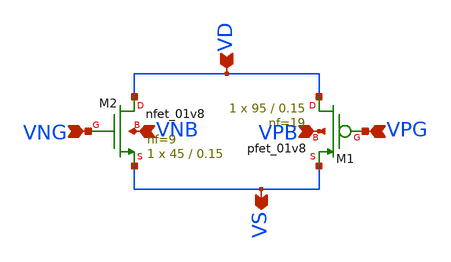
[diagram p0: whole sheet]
** sch_path: SP23_Tapeout/C2S2_Analog_TestChip-main/xschem/a_mux_switch.sch
**.subckt a_mux_switch VPG VNG VD VS VPB VNB
*.ipin VPG
*.ipin VNG
*.ipin VD
*.opin VS
*.ipin VPB
*.ipin VNB
XM1 VD VPG VS VPB sky130_fd_pr__pfet_01v8 L=0.15 W=95 nf=19 ad='int((nf+1)/2) * W/nf * 0.29' as='int((nf+2)/2) * W/nf * 0.29'
+ pd='2*int((nf+1)/2) * (W/nf + 0.29)' ps='2*int((nf+2)/2) * (W/nf + 0.29)' nrd='0.29 / W' nrs='0.29 / W'
+ sa=0 sb=0 sd=0 mult=1 m=1
XM2 VD VNG VS VNB sky130_fd_pr__nfet_01v8 L=0.15 W=45 nf=9 ad='int((nf+1)/2) * W/nf * 0.29' as='int((nf+2)/2) * W/nf * 0.29'
+ pd='2*int((nf+1)/2) * (W/nf + 0.29)' ps='2*int((nf+2)/2) * (W/nf + 0.29)' nrd='0.29 / W' nrs='0.29 / W'
+ sa=0 sb=0 sd=0 mult=1 m=1
**.ends
.end
